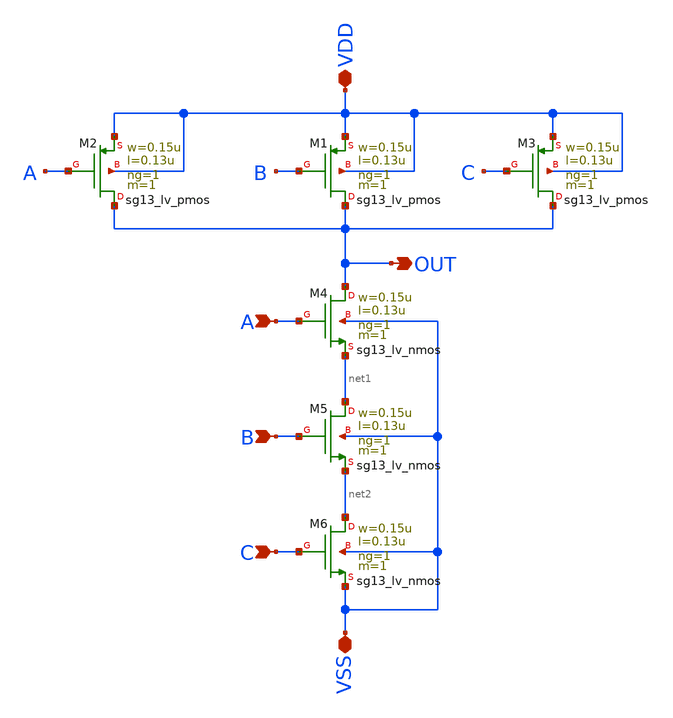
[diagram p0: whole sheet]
** sch_path: CDR4176-main/schematic/xschem/nand_x3_custom/nand_x3_custom.sch
**.subckt nand_x3_custom A B C VSS VDD OUT
*.ipin A
*.ipin B
*.ipin C
*.iopin VSS
*.iopin VDD
*.opin OUT
XM2 OUT A VDD VDD sg13_lv_pmos w=0.15u l=0.13u ng=1 m=1 mm_ok=1
XM1 OUT B VDD VDD sg13_lv_pmos w=0.15u l=0.13u ng=1 m=1 mm_ok=1
XM3 OUT C VDD VDD sg13_lv_pmos w=0.15u l=0.13u ng=1 m=1 mm_ok=1
XM4 OUT A net1 VSS sg13_lv_nmos w=0.15u l=0.13u ng=1 m=1 mm_ok=1
XM5 net1 B net2 VSS sg13_lv_nmos w=0.15u l=0.13u ng=1 m=1 mm_ok=1
XM6 net2 C VSS VSS sg13_lv_nmos w=0.15u l=0.13u ng=1 m=1 mm_ok=1
**.ends
.end
